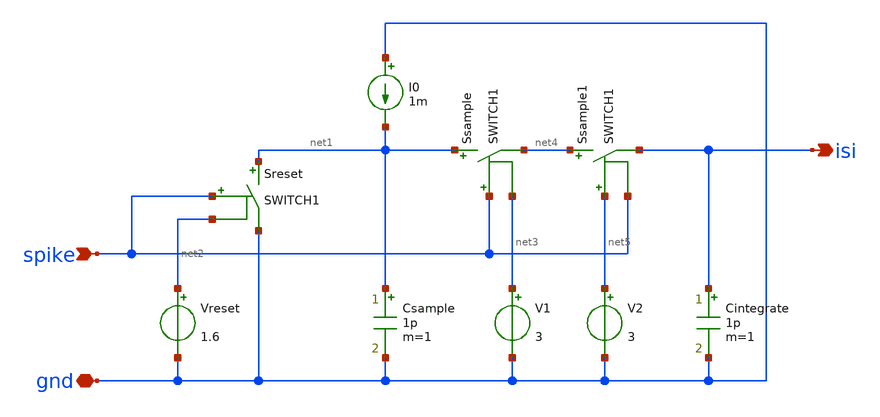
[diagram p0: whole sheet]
** sch_path: playground/InterServicesIntelligence.sch
**.subckt InterServicesIntelligence gnd spike isi
*.iopin gnd
*.ipin spike
*.opin isi
Csample net1 gnd 1p m=1
I0 gnd net1 1m
Ssample net1 net4 spike net3 SWITCH1
Sreset net1 gnd spike net2 SWITCH1
Cintegrate isi gnd 1p m=1
V1 net3 gnd 3
Vreset net2 gnd 1.6
Ssample1 net4 isi net5 spike SWITCH1
V2 net5 gnd 3
**.ends
.end
